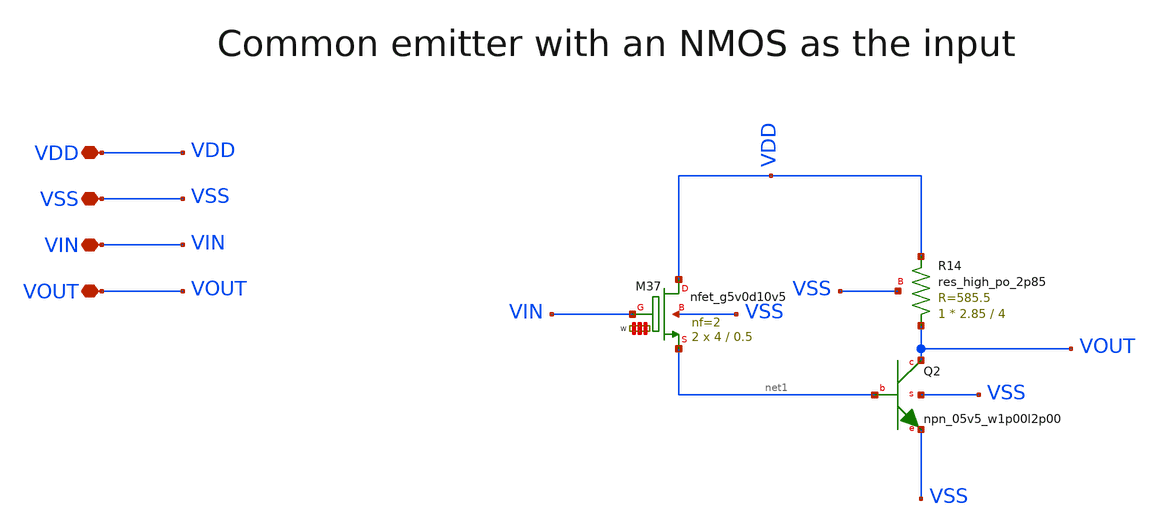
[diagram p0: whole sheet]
** sch_path: LIB/Sky130A/primordial_bicmos/audio001_5V_sky130A.sch
**.subckt audio001_5V_sky130A VDD VSS VIN VOUT
*.iopin VDD
*.iopin VSS
*.iopin VIN
*.iopin VOUT
XM37 VDD VIN net1 VSS sky130_fd_pr__nfet_g5v0d10v5 L=0.5 W='4 * 2 ' nf=2 ad='int((nf+1)/2) * W / nf * 0.29'
+ as='int((nf+2)/2) * W / nf * 0.29' pd='2*int((nf+1)/2) * (W / nf + 0.29)' ps='2*int((nf+2)/2) * (W / nf + 0.29)'
+ nrd='0.29 / W ' nrs='0.29 / W ' sa=0 sb=0 sd=0 mult=2 m=2
XQ2 VOUT net1 VSS VSS sky130_fd_pr__npn_05v5_w1p00l2p00
XR14 VOUT VDD VSS sky130_fd_pr__res_high_po_2p85 L=4 mult=1 m=1
**.ends
.end
